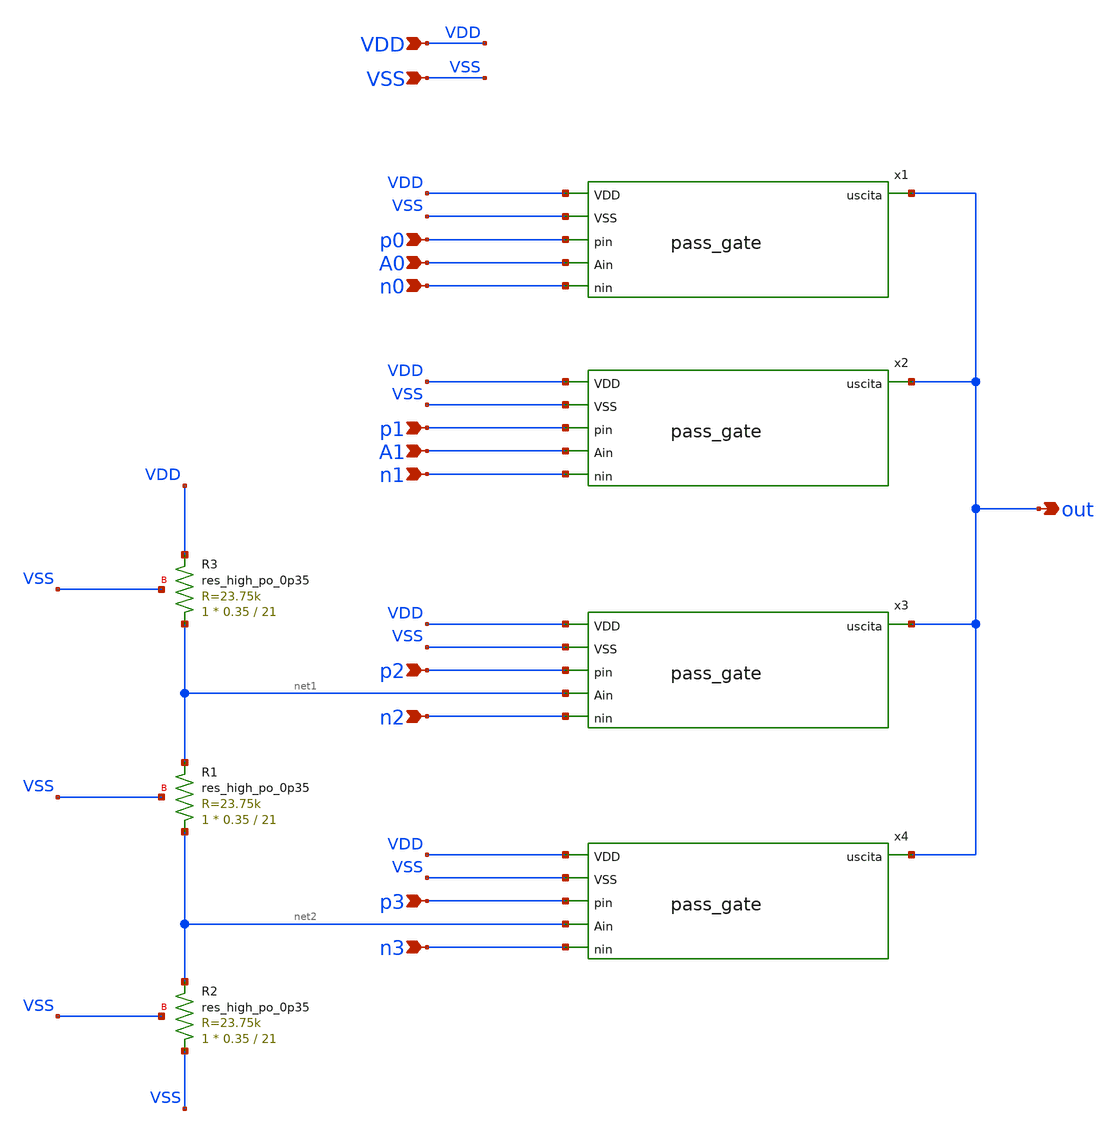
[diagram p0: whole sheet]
** sch_path: xschem/Mux.sch
**.subckt Mux A0 out p0 A1 p1 n0 p2 n2 n1 p3 n3 VDD VSS
*.ipin A0
*.opin out
*.ipin p0
*.ipin A1
*.ipin p1
*.ipin n0
*.ipin p2
*.ipin n2
*.ipin n1
*.ipin p3
*.ipin n3
*.ipin VDD
*.ipin VSS
x1 VDD VSS p0 A0 out n0 pass_gate
x2 VDD VSS p1 A1 out n1 pass_gate
x3 VDD VSS p2 net1 out n2 pass_gate
x4 VDD VSS p3 net2 out n3 pass_gate
XR3 net1 VDD VSS sky130_fd_pr__res_high_po_0p35 L=21 mult=1 m=1
XR1 net2 net1 VSS sky130_fd_pr__res_high_po_0p35 L=21 mult=1 m=1
XR2 VSS net2 VSS sky130_fd_pr__res_high_po_0p35 L=21 mult=1 m=1
**.ends

* expanding   symbol:  pass_gate.sym # of pins=6
** sym_path: xschem/pass_gate.sym
** sch_path: xschem/pass_gate.sch
.subckt pass_gate VDD VSS pin Ain uscita nin
*.ipin Ain
*.ipin pin
*.ipin nin
*.ipin VDD
*.ipin VSS
*.opin uscita
XM2 Ain nin uscita VSS sky130_fd_pr__nfet_01v8_lvt L=0.15 W=8 nf=8 ad='int((nf+1)/2) * W/nf * 0.29' as='int((nf+2)/2) * W/nf * 0.29'
+ pd='2*int((nf+1)/2) * (W/nf + 0.29)' ps='2*int((nf+2)/2) * (W/nf + 0.29)' nrd='0.29 / W' nrs='0.29 / W'
+ sa=0 sb=0 sd=0 mult=1 m=1
XM3 uscita pin Ain VDD sky130_fd_pr__pfet_01v8_lvt L=0.35 W=16 nf=16 ad='int((nf+1)/2) * W/nf * 0.29'
+ as='int((nf+2)/2) * W/nf * 0.29' pd='2*int((nf+1)/2) * (W/nf + 0.29)' ps='2*int((nf+2)/2) * (W/nf + 0.29)'
+ nrd='0.29 / W' nrs='0.29 / W' sa=0 sb=0 sd=0 mult=1 m=1
.ends

.end
